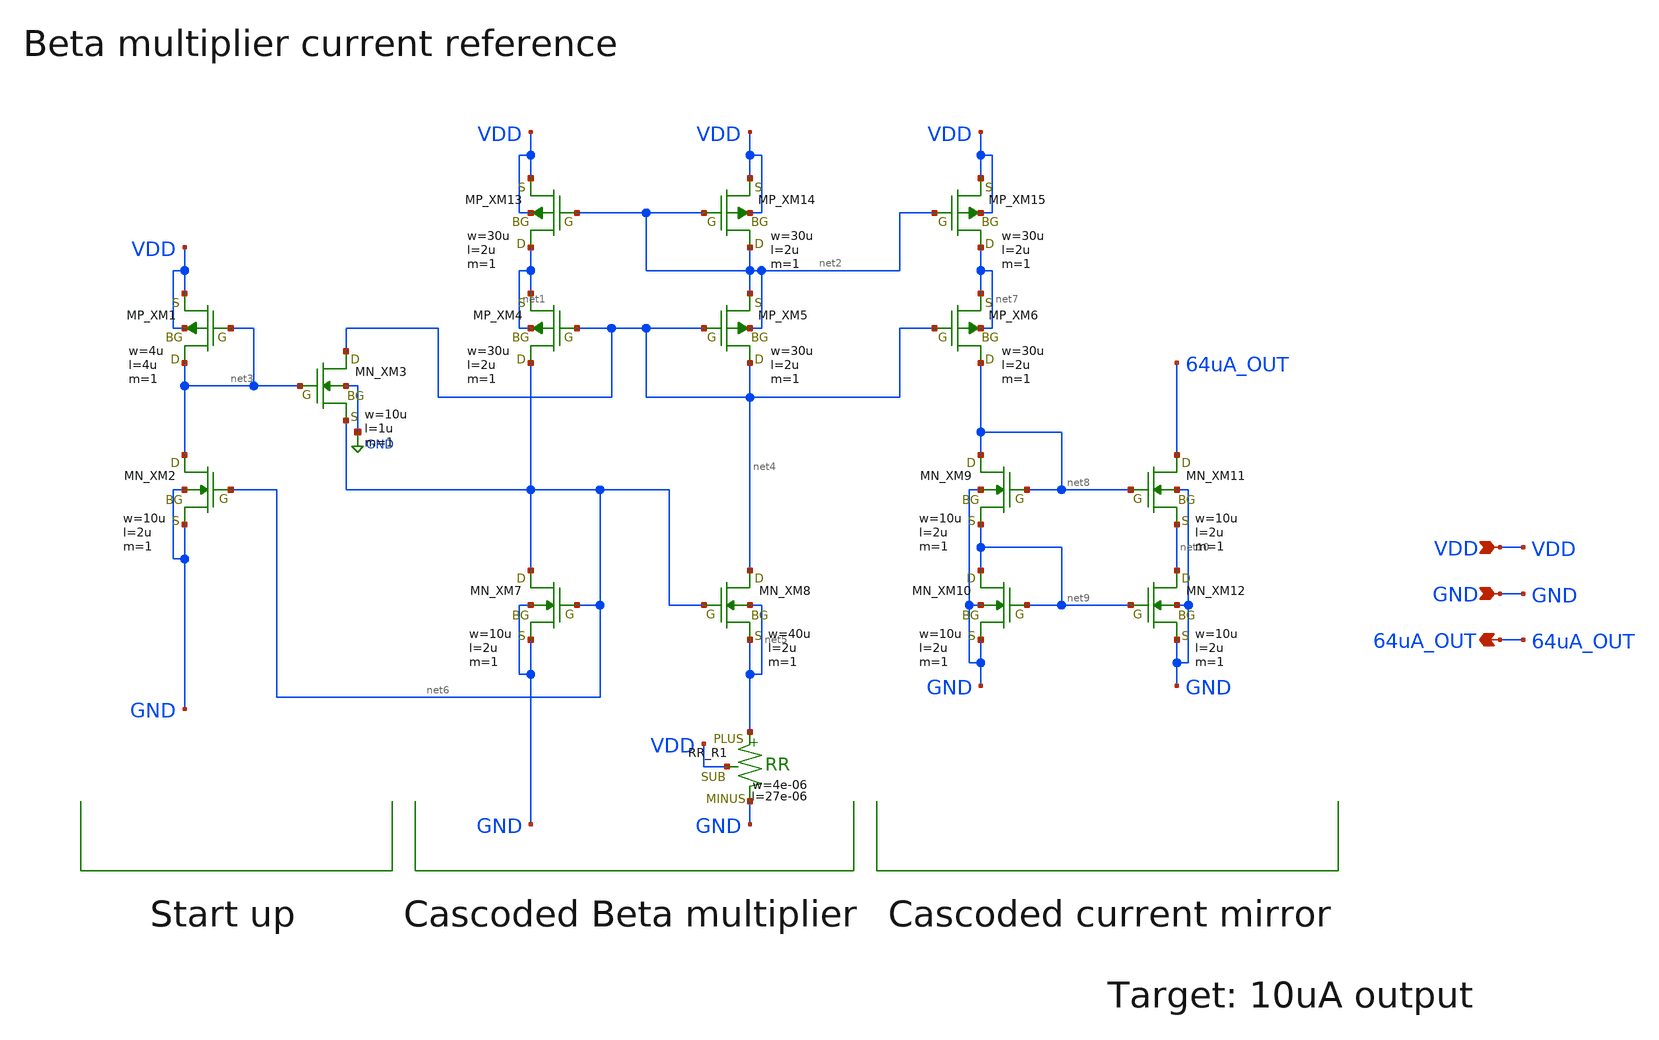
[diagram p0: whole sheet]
** sch_path: member_project/AM_Radio/Yamada3/xschem/bmr.sch
* Copyright 2022 GlobalFoundries PDK Authors
* Licensed under the Apache License, Version 2.0 (the "License");
* you may not use this file except in compliance with the License.
* You may obtain a copy of the License at
* https://www.apache.org/licenses/LICENSE-2.0
* Unless required by applicable law or agreed to in writing, software
* distributed under the License is distributed on an "AS IS" BASIS,
* WITHOUT WARRANTIES OR CONDITIONS OF ANY KIND, either express or implied.
* See the License for the specific language governing permissions and
* limitations under the License.
**.subckt bmr VDD GND 64uA_OUT
*.ipin VDD
*.ipin GND
*.opin 64uA_OUT
XXM1 net3 net3 VDD VDD PMOS w=4u l=4u as=0 ad=0 ps=0 pd=0 nrd=0 nrs=0 m=1
XXM2 net3 net6 GND GND NMOS w=10u l=2u as=0 ad=0 ps=0 pd=0 nrd=0 nrs=0 m=1
XXM3 net4 net3 net6 GND NMOS w=10u l=1u as=0 ad=0 ps=0 pd=0 nrd=0 nrs=0 m=1
XXM4 net6 net4 net1 net1 PMOS w=30u l=2u as=0 ad=0 ps=0 pd=0 nrd=0 nrs=0 m=1
XXM5 net4 net4 net2 net2 PMOS w=30u l=2u as=0 ad=0 ps=0 pd=0 nrd=0 nrs=0 m=1
XXM7 net6 net6 GND GND NMOS w=10u l=2u as=0 ad=0 ps=0 pd=0 nrd=0 nrs=0 m=1
XXM8 net4 net6 net5 net5 NMOS w=40u l=2u as=0 ad=0 ps=0 pd=0 nrd=0 nrs=0 m=1
XR1 net5 GND VDD F_RR w=4e-06 R=1 l=27e-06 tc1=0 tc2=0
XXM6 net8 net4 net7 net7 PMOS w=30u l=2u as=0 ad=0 ps=0 pd=0 nrd=0 nrs=0 m=1
XXM9 net8 net8 net9 GND NMOS w=10u l=2u as=0 ad=0 ps=0 pd=0 nrd=0 nrs=0 m=1
XXM10 net9 net9 GND GND NMOS w=10u l=2u as=0 ad=0 ps=0 pd=0 nrd=0 nrs=0 m=1
XXM11 64uA_OUT net8 net10 GND NMOS w=10u l=2u as=0 ad=0 ps=0 pd=0 nrd=0 nrs=0 m=1
XXM12 net10 net9 GND GND NMOS w=10u l=2u as=0 ad=0 ps=0 pd=0 nrd=0 nrs=0 m=1
XXM13 net1 net2 VDD VDD PMOS w=30u l=2u as=0 ad=0 ps=0 pd=0 nrd=0 nrs=0 m=1
XXM14 net2 net2 VDD VDD PMOS w=30u l=2u as=0 ad=0 ps=0 pd=0 nrd=0 nrs=0 m=1
XXM15 net7 net2 VDD VDD PMOS w=30u l=2u as=0 ad=0 ps=0 pd=0 nrd=0 nrs=0 m=1
**.ends
.GLOBAL GND
.end
